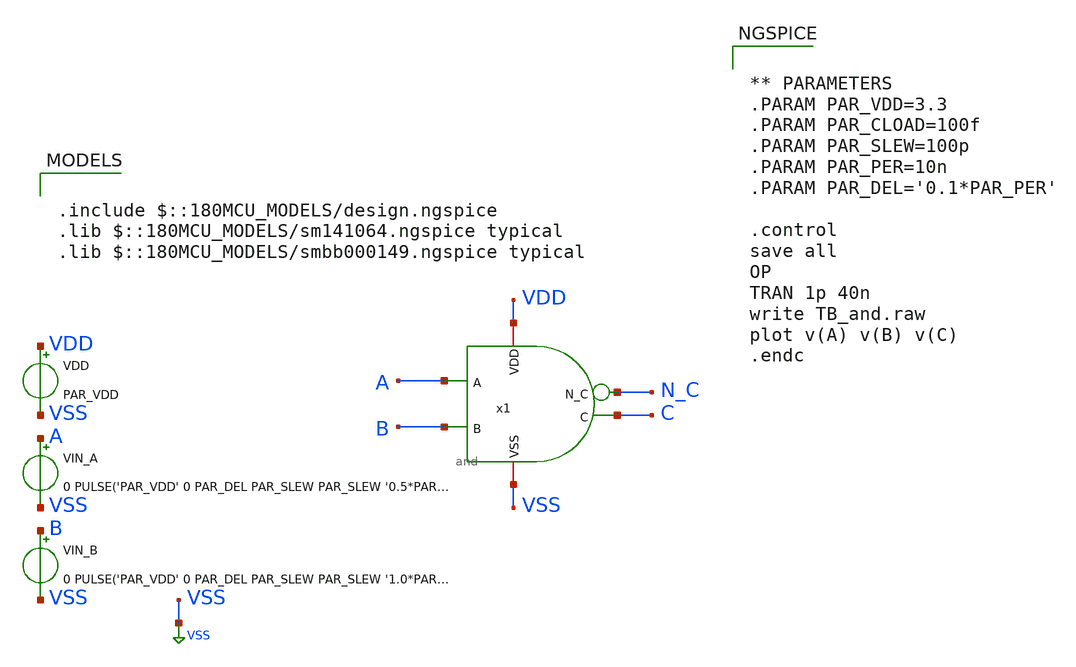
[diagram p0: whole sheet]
** sch_path: schematics/logic-gates/and/and_tb.sch
**.subckt and_tb
VIN_A A VSS 0 PULSE('PAR_VDD' 0 PAR_DEL PAR_SLEW PAR_SLEW '0.5*PAR_PER' '1.0*PAR_PER')
VDD VDD VSS PAR_VDD
x1 A B N_C C VDD VSS and
VIN_B B VSS 0 PULSE('PAR_VDD' 0 PAR_DEL PAR_SLEW PAR_SLEW '1.0*PAR_PER' '2.0*PAR_PER')
**** begin user architecture code

.include $::180MCU_MODELS/design.ngspice
.lib $::180MCU_MODELS/sm141064.ngspice typical
.lib $::180MCU_MODELS/smbb000149.ngspice typical



** PARAMETERS
.PARAM PAR_VDD=3.3
.PARAM PAR_CLOAD=100f
.PARAM PAR_SLEW=100p
.PARAM PAR_PER=10n
.PARAM PAR_DEL='0.1*PAR_PER'

.control
save all
OP
TRAN 1p 40n
write TB_and.raw
plot v(A) v(B) v(C)
.endc



**** end user architecture code
**.ends

* expanding   symbol:  schematics/logic-gates/and/and.sym # of pins=6
** sym_path: schematics/logic-gates/and/and.sym
** sch_path: schematics/logic-gates/and/and.sch
.subckt and A B N_C C VDD VSS
*.ipin A
*.ipin B
*.opin C
*.opin N_C
*.iopin VDD
*.iopin VSS
XM1 N_C B net1 VSS nfet_03v3 L=0.28u W=0.22u nf=1 ad='int((nf+1)/2) * W/nf * 0.18u' as='int((nf+2)/2) * W/nf * 0.18u'
+ pd='2*int((nf+1)/2) * (W/nf + 0.18u)' ps='2*int((nf+2)/2) * (W/nf + 0.18u)' nrd='0.18u / W' nrs='0.18u / W'
+ sa=0 sb=0 sd=0 m=1
XM2 N_C A VDD VDD pfet_03v3 L=0.28u W=0.22u nf=1 ad='int((nf+1)/2) * W/nf * 0.18u' as='int((nf+2)/2) * W/nf * 0.18u'
+ pd='2*int((nf+1)/2) * (W/nf + 0.18u)' ps='2*int((nf+2)/2) * (W/nf + 0.18u)' nrd='0.18u / W' nrs='0.18u / W'
+ sa=0 sb=0 sd=0 m=1
XM3 N_C B VDD VDD pfet_03v3 L=0.28u W=0.22u nf=1 ad='int((nf+1)/2) * W/nf * 0.18u' as='int((nf+2)/2) * W/nf * 0.18u'
+ pd='2*int((nf+1)/2) * (W/nf + 0.18u)' ps='2*int((nf+2)/2) * (W/nf + 0.18u)' nrd='0.18u / W' nrs='0.18u / W'
+ sa=0 sb=0 sd=0 m=1
XM4 net1 A VSS VSS nfet_03v3 L=0.28u W=0.22u nf=1 ad='int((nf+1)/2) * W/nf * 0.18u' as='int((nf+2)/2) * W/nf * 0.18u'
+ pd='2*int((nf+1)/2) * (W/nf + 0.18u)' ps='2*int((nf+2)/2) * (W/nf + 0.18u)' nrd='0.18u / W' nrs='0.18u / W'
+ sa=0 sb=0 sd=0 m=1
XM5 C N_C VDD VDD pfet_03v3 L=0.28u W=0.22u nf=1 ad='int((nf+1)/2) * W/nf * 0.18u' as='int((nf+2)/2) * W/nf * 0.18u'
+ pd='2*int((nf+1)/2) * (W/nf + 0.18u)' ps='2*int((nf+2)/2) * (W/nf + 0.18u)' nrd='0.18u / W' nrs='0.18u / W'
+ sa=0 sb=0 sd=0 m=1
XM6 C N_C VSS VSS nfet_03v3 L=0.28u W=0.22u nf=1 ad='int((nf+1)/2) * W/nf * 0.18u' as='int((nf+2)/2) * W/nf * 0.18u'
+ pd='2*int((nf+1)/2) * (W/nf + 0.18u)' ps='2*int((nf+2)/2) * (W/nf + 0.18u)' nrd='0.18u / W' nrs='0.18u / W'
+ sa=0 sb=0 sd=0 m=1
.ends

.GLOBAL VSS
.end
